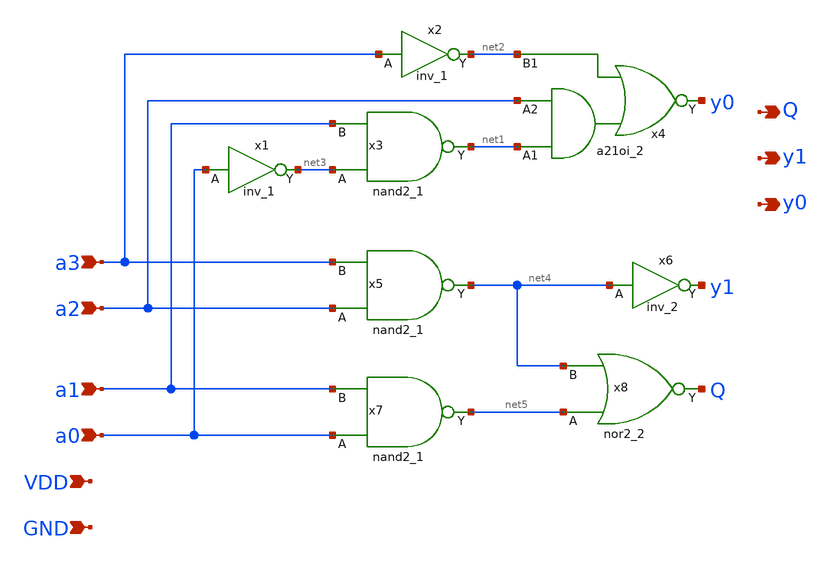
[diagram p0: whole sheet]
** sch_path: BNE_4bit.sch
**.subckt BNE_4bit a1 a0 y1 y0 a3 a2 Q VDD GND
*.ipin a1
*.ipin a0
*.opin y1
*.opin y0
*.ipin a3
*.ipin a2
*.opin Q
*.ipin VDD
*.ipin GND
x1 a0 GND GND VDD VDD net3 sky130_fd_sc_hd__inv_1
x2 a3 GND GND VDD VDD net2 sky130_fd_sc_hd__inv_1
x3 net3 a1 GND GND VDD VDD net1 sky130_fd_sc_hd__nand2_1
x4 net1 a2 net2 GND GND VDD VDD y0 sky130_fd_sc_hd__a21oi_2
x5 a2 a3 GND GND VDD VDD net4 sky130_fd_sc_hd__nand2_1
x6 net4 GND GND VDD VDD y1 sky130_fd_sc_hd__inv_2
x7 a0 a1 GND GND VDD VDD net5 sky130_fd_sc_hd__nand2_1
x8 net5 net4 GND GND VDD VDD Q sky130_fd_sc_hd__nor2_2
**.ends
.end
